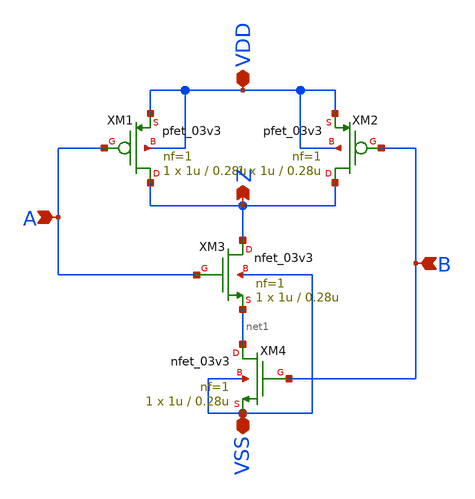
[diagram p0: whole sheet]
** sch_path: sar_logic/sar_designs/nand2.sch
**.subckt nand2 A B VSS VDD Z
*.ipin A
*.ipin B
*.iopin VSS
*.iopin VDD
*.opin Z
XM1 Z A VDD VDD pfet_03v3 L=0.28u W=1u nf=1 ad='int((nf+1)/2) * W/nf * 0.18u' as='int((nf+2)/2) * W/nf * 0.18u'
+ pd='2*int((nf+1)/2) * (W/nf + 0.18u)' ps='2*int((nf+2)/2) * (W/nf + 0.18u)' nrd='0.18u / W' nrs='0.18u / W'
+ sa=0 sb=0 sd=0 m=1
XM2 Z B VDD VDD pfet_03v3 L=0.28u W=1u nf=1 ad='int((nf+1)/2) * W/nf * 0.18u' as='int((nf+2)/2) * W/nf * 0.18u'
+ pd='2*int((nf+1)/2) * (W/nf + 0.18u)' ps='2*int((nf+2)/2) * (W/nf + 0.18u)' nrd='0.18u / W' nrs='0.18u / W'
+ sa=0 sb=0 sd=0 m=1
XM3 Z A net1 VSS nfet_03v3 L=0.28u W=1u nf=1 ad='int((nf+1)/2) * W/nf * 0.18u' as='int((nf+2)/2) * W/nf * 0.18u'
+ pd='2*int((nf+1)/2) * (W/nf + 0.18u)' ps='2*int((nf+2)/2) * (W/nf + 0.18u)' nrd='0.18u / W' nrs='0.18u / W'
+ sa=0 sb=0 sd=0 m=1
XM4 net1 B VSS VSS nfet_03v3 L=0.28u W=1u nf=1 ad='int((nf+1)/2) * W/nf * 0.18u' as='int((nf+2)/2) * W/nf * 0.18u'
+ pd='2*int((nf+1)/2) * (W/nf + 0.18u)' ps='2*int((nf+2)/2) * (W/nf + 0.18u)' nrd='0.18u / W' nrs='0.18u / W'
+ sa=0 sb=0 sd=0 m=1
**.ends
.end
